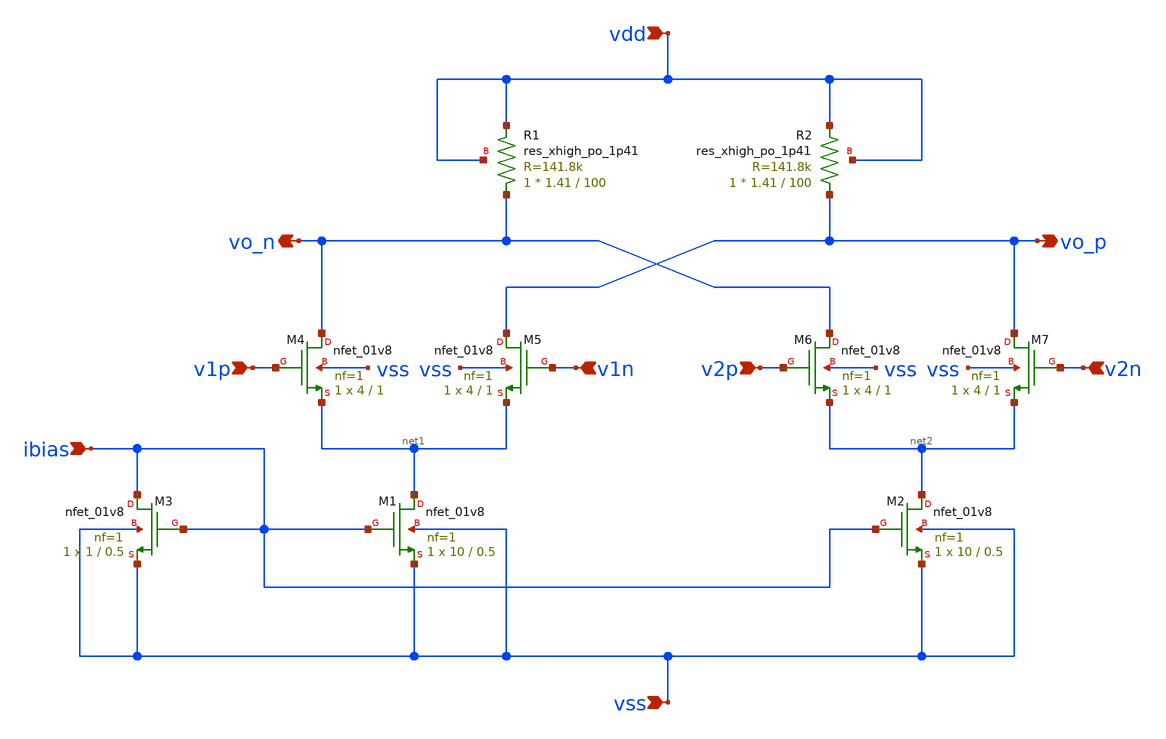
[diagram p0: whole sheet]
** sch_path: sch/diff_diff_amp.sch
**.subckt diff_diff_amp v1p v1n v2p v2n vss vdd ibias vo_n vo_p
*.ipin v1p
*.ipin v1n
*.ipin v2p
*.ipin v2n
*.ipin vss
*.ipin vdd
*.ipin ibias
*.opin vo_n
*.opin vo_p
XM1 net1 ibias vss vss sky130_fd_pr__nfet_01v8 L=0.5 W=10 nf=1 ad='int((nf+1)/2) * W/nf * 0.29' as='int((nf+2)/2) * W/nf * 0.29'
+ pd='2*int((nf+1)/2) * (W/nf + 0.29)' ps='2*int((nf+2)/2) * (W/nf + 0.29)' nrd='0.29 / W' nrs='0.29 / W'
+ sa=0 sb=0 sd=0 mult=1 m=1
XM2 net2 ibias vss vss sky130_fd_pr__nfet_01v8 L=0.5 W=10 nf=1 ad='int((nf+1)/2) * W/nf * 0.29' as='int((nf+2)/2) * W/nf * 0.29'
+ pd='2*int((nf+1)/2) * (W/nf + 0.29)' ps='2*int((nf+2)/2) * (W/nf + 0.29)' nrd='0.29 / W' nrs='0.29 / W'
+ sa=0 sb=0 sd=0 mult=1 m=1
XM3 ibias ibias vss vss sky130_fd_pr__nfet_01v8 L=0.5 W=1 nf=1 ad='int((nf+1)/2) * W/nf * 0.29' as='int((nf+2)/2) * W/nf * 0.29'
+ pd='2*int((nf+1)/2) * (W/nf + 0.29)' ps='2*int((nf+2)/2) * (W/nf + 0.29)' nrd='0.29 / W' nrs='0.29 / W'
+ sa=0 sb=0 sd=0 mult=1 m=1
XM4 vo_n v1p net1 vss sky130_fd_pr__nfet_01v8 L=1 W=4 nf=1 ad='int((nf+1)/2) * W/nf * 0.29' as='int((nf+2)/2) * W/nf * 0.29'
+ pd='2*int((nf+1)/2) * (W/nf + 0.29)' ps='2*int((nf+2)/2) * (W/nf + 0.29)' nrd='0.29 / W' nrs='0.29 / W'
+ sa=0 sb=0 sd=0 mult=1 m=1
XM5 vo_p v1n net1 vss sky130_fd_pr__nfet_01v8 L=1 W=4 nf=1 ad='int((nf+1)/2) * W/nf * 0.29' as='int((nf+2)/2) * W/nf * 0.29'
+ pd='2*int((nf+1)/2) * (W/nf + 0.29)' ps='2*int((nf+2)/2) * (W/nf + 0.29)' nrd='0.29 / W' nrs='0.29 / W'
+ sa=0 sb=0 sd=0 mult=1 m=1
XM6 vo_n v2p net2 vss sky130_fd_pr__nfet_01v8 L=1 W=4 nf=1 ad='int((nf+1)/2) * W/nf * 0.29' as='int((nf+2)/2) * W/nf * 0.29'
+ pd='2*int((nf+1)/2) * (W/nf + 0.29)' ps='2*int((nf+2)/2) * (W/nf + 0.29)' nrd='0.29 / W' nrs='0.29 / W'
+ sa=0 sb=0 sd=0 mult=1 m=1
XM7 vo_p v2n net2 vss sky130_fd_pr__nfet_01v8 L=1 W=4 nf=1 ad='int((nf+1)/2) * W/nf * 0.29' as='int((nf+2)/2) * W/nf * 0.29'
+ pd='2*int((nf+1)/2) * (W/nf + 0.29)' ps='2*int((nf+2)/2) * (W/nf + 0.29)' nrd='0.29 / W' nrs='0.29 / W'
+ sa=0 sb=0 sd=0 mult=1 m=1
XR1 vo_n vdd vdd sky130_fd_pr__res_xhigh_po_1p41 L=100 mult=1 m=1
XR2 vo_p vdd vdd sky130_fd_pr__res_xhigh_po_1p41 L=100 mult=1 m=1
**.ends
.end
